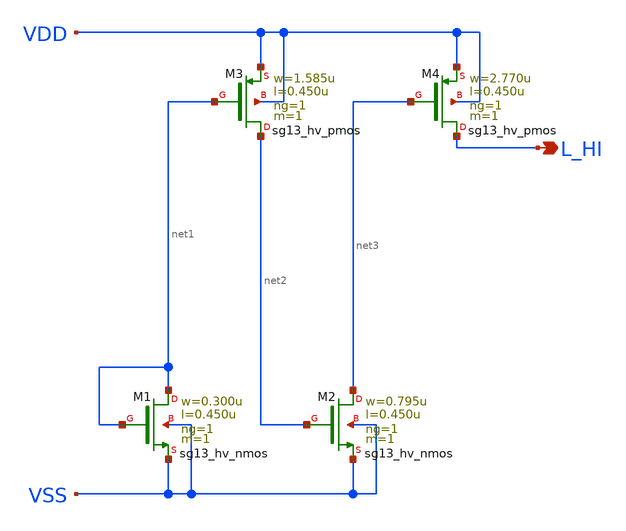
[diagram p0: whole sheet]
** sch_path: sch/xschem/sg13g2_hv_tiehi.sch
* Copyright 2023 IHP PDK Authors
* Licensed under the Apache License, Version 2.0 (the "License");
* you may not use this file except in compliance with the License.
* You may obtain a copy of the License at
* https://www.apache.org/licenses/LICENSE-2.0
* Unless required by applicable law or agreed to in writing, software
* distributed under the License is distributed on an "AS IS" BASIS,
* WITHOUT WARRANTIES OR CONDITIONS OF ANY KIND, either express or implied.
* See the License for the specific language governing permissions and
* limitations under the License.
**.subckt sg13g2_hv_tiehi L_HI
*.opin L_HI
XM1 net1 net1 VSS VSS sg13_hv_nmos w=0.300u l=0.450u ng=1 m=1 mm_ok=1
XM2 net3 net2 VSS VSS sg13_hv_nmos w=0.795u l=0.450u ng=1 m=1 mm_ok=1
XM3 net2 net1 VDD VDD sg13_hv_pmos w=1.585u l=0.450u ng=1 m=1 mm_ok=1
XM4 L_HI net3 VDD VDD sg13_hv_pmos w=2.770u l=0.450u ng=1 m=1 mm_ok=1
**.ends
.end
